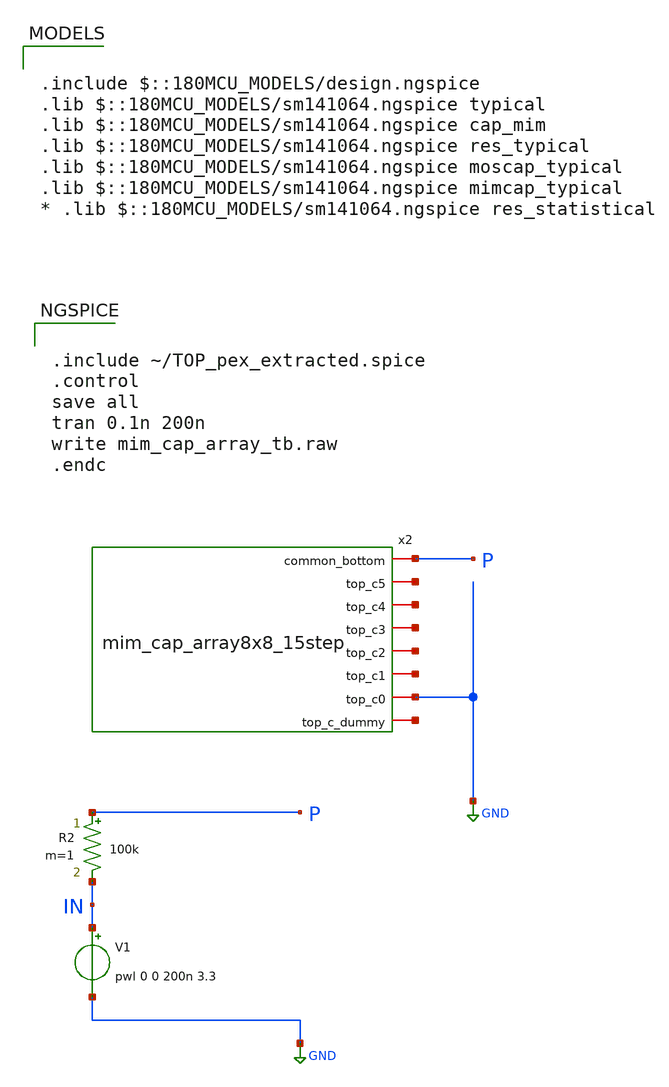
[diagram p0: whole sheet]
** sch_path: cdac/mim_cap_array_8x8/mim_cap_array_tb.sch
* Copyright 2022 GlobalFoundries PDK Authors
* Licensed under the Apache License, Version 2.0 (the "License");
* you may not use this file except in compliance with the License.
* You may obtain a copy of the License at
* https://www.apache.org/licenses/LICENSE-2.0
* Unless required by applicable law or agreed to in writing, software
* distributed under the License is distributed on an "AS IS" BASIS,
* WITHOUT WARRANTIES OR CONDITIONS OF ANY KIND, either express or implied.
* See the License for the specific language governing permissions and
* limitations under the License.
**.subckt mim_cap_array_tb
V1 IN GND pwl 0 0 200n 3.3
R2 P IN 100k m=1
x2 P net4 net3 net2 net1 net6 net5 GND TOP
**** begin user architecture code

.include $::180MCU_MODELS/design.ngspice
.lib $::180MCU_MODELS/sm141064.ngspice typical
.lib $::180MCU_MODELS/sm141064.ngspice cap_mim
.lib $::180MCU_MODELS/sm141064.ngspice res_typical
.lib $::180MCU_MODELS/sm141064.ngspice moscap_typical
.lib $::180MCU_MODELS/sm141064.ngspice mimcap_typical
* .lib $::180MCU_MODELS/sm141064.ngspice res_statistical



.include ~/TOP_pex_extracted.spice
.control
save all
tran 0.1n 200n
write mim_cap_array_tb.raw
.endc


**** end user architecture code
**.ends
.GLOBAL GND
.end
